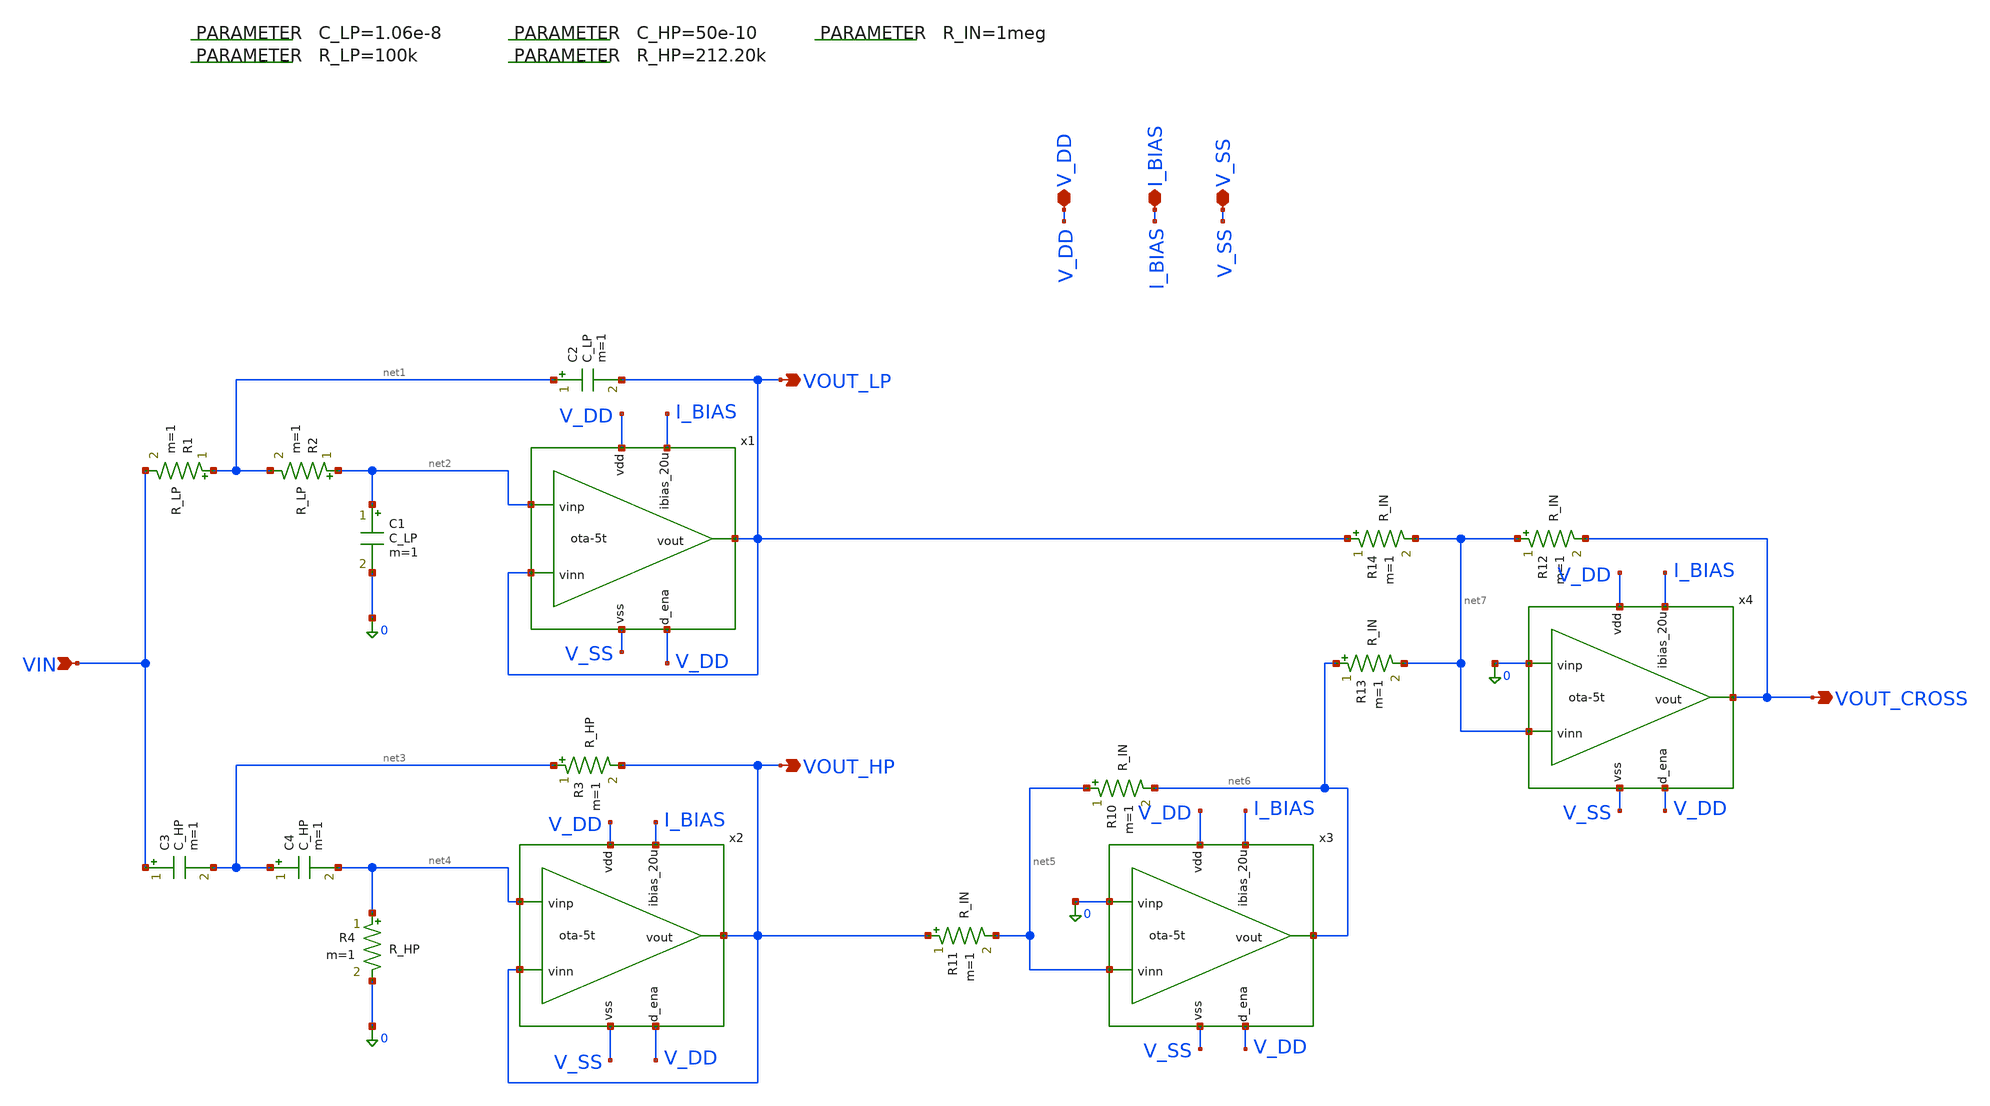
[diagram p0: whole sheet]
** sch_path: 004_Real_Circuits/001_version_basic_ota_pretl/linkwtz_riley_crossover_pretl_OTA.sch
* 004_Real_Circuits/001_version_basic_ota_pretl/ota-5t.sch:
* (c) 2024-2025 Harald Pretl, Apache-2.0 license
**.subckt linkwtz_riley_crossover_pretl_OTA VOUT_LP VOUT_HP VIN VOUT_CROSS V_DD I_BIAS V_SS
*.opin VOUT_LP
*.opin VOUT_HP
*.ipin VIN
*.opin VOUT_CROSS
*.iopin V_DD
*.iopin I_BIAS
*.iopin V_SS
R1 net1 VIN R_LP m=1
R2 net2 net1 R_LP m=1
C1 net2 0 C_LP m=1
C2 net1 VOUT_LP C_LP m=1
C3 VIN net3 C_HP m=1
C4 net3 net4 C_HP m=1
R3 net3 VOUT_HP R_HP m=1
R4 net4 0 R_HP m=1
R10 net5 net6 R_IN m=1
R11 VOUT_HP net5 R_IN m=1
R12 net7 VOUT_CROSS R_IN m=1
R13 net6 net7 R_IN m=1
R14 VOUT_LP net7 R_IN m=1
x1 V_DD VOUT_LP net2 VOUT_LP I_BIAS V_DD V_SS ota-5t
x2 V_DD VOUT_HP net4 VOUT_HP I_BIAS V_DD V_SS ota-5t
x3 V_DD net6 0 net5 I_BIAS V_DD V_SS ota-5t
x4 V_DD VOUT_CROSS 0 net7 I_BIAS V_DD V_SS ota-5t
.param C_LP=1.06e-8
.param R_LP=100k
.param C_HP=50e-10
.param R_HP=212.20k
.param R_IN=1meg
**.ends

* expanding   symbol:  004_Real_Circuits/001_version_basic_ota_pretl/ota-5t.sym # of pins=7
** sym_path: 004_Real_Circuits/001_version_basic_ota_pretl/ota-5t.sym
** sch_path: 004_Real_Circuits/001_version_basic_ota_pretl/ota-5t.sch
.subckt ota-5t vdd vout vinp vinn ibias_20u d_ena vss
*.ipin ibias_20u
*.iopin vdd
*.iopin vss
*.ipin vinp
*.ipin vinn
*.opin vout
*.ipin d_ena
XM5 tail gate_n vss vss sg13_lv_nmos w=1.5u l=5u ng=1 m=1 mm_ok=1
XM4 vout gate_p vdd vdd sg13_lv_pmos w=3.5u l=5u ng=1 m=1 mm_ok=1
XM1 gate_p vinp tail vss sg13_lv_nmos w=2u l=5u ng=1 m=1 mm_ok=1
XM2 vout vinn tail vss sg13_lv_nmos w=2u l=5u ng=1 m=1 mm_ok=1
XM3 gate_p gate_p vdd vdd sg13_lv_pmos w=3.5u l=5u ng=1 m=1 mm_ok=1
XM6 ibias_20u gate_n vss vss sg13_lv_nmos w=10u l=5u ng=5 m=1 mm_ok=1
XM9 gate_n ena_n vss vss sg13_lv_nmos w=0.5u l=0.13u ng=1 m=1 mm_ok=1
XM11 gate_p ena vdd vdd sg13_lv_pmos w=1.5u l=0.13u ng=1 m=1 mm_ok=1
XM7 ena ena_n vss vss sg13_lv_nmos w=0.5u l=0.13u ng=1 m=1 mm_ok=1
XM8 ena ena_n vdd vdd sg13_lv_pmos w=1.5u l=0.13u ng=1 m=1 mm_ok=1
XM10 ibias_20u ena gate_n vss sg13_lv_nmos w=0.5u l=0.13u ng=1 m=1 mm_ok=1
XM12 ena_n d_ena vss vss sg13_lv_nmos w=0.5u l=0.13u ng=1 m=1 mm_ok=1
XM13 ena_n d_ena vdd vdd sg13_lv_pmos w=1.5u l=0.13u ng=1 m=1 mm_ok=1
.ends

.end
